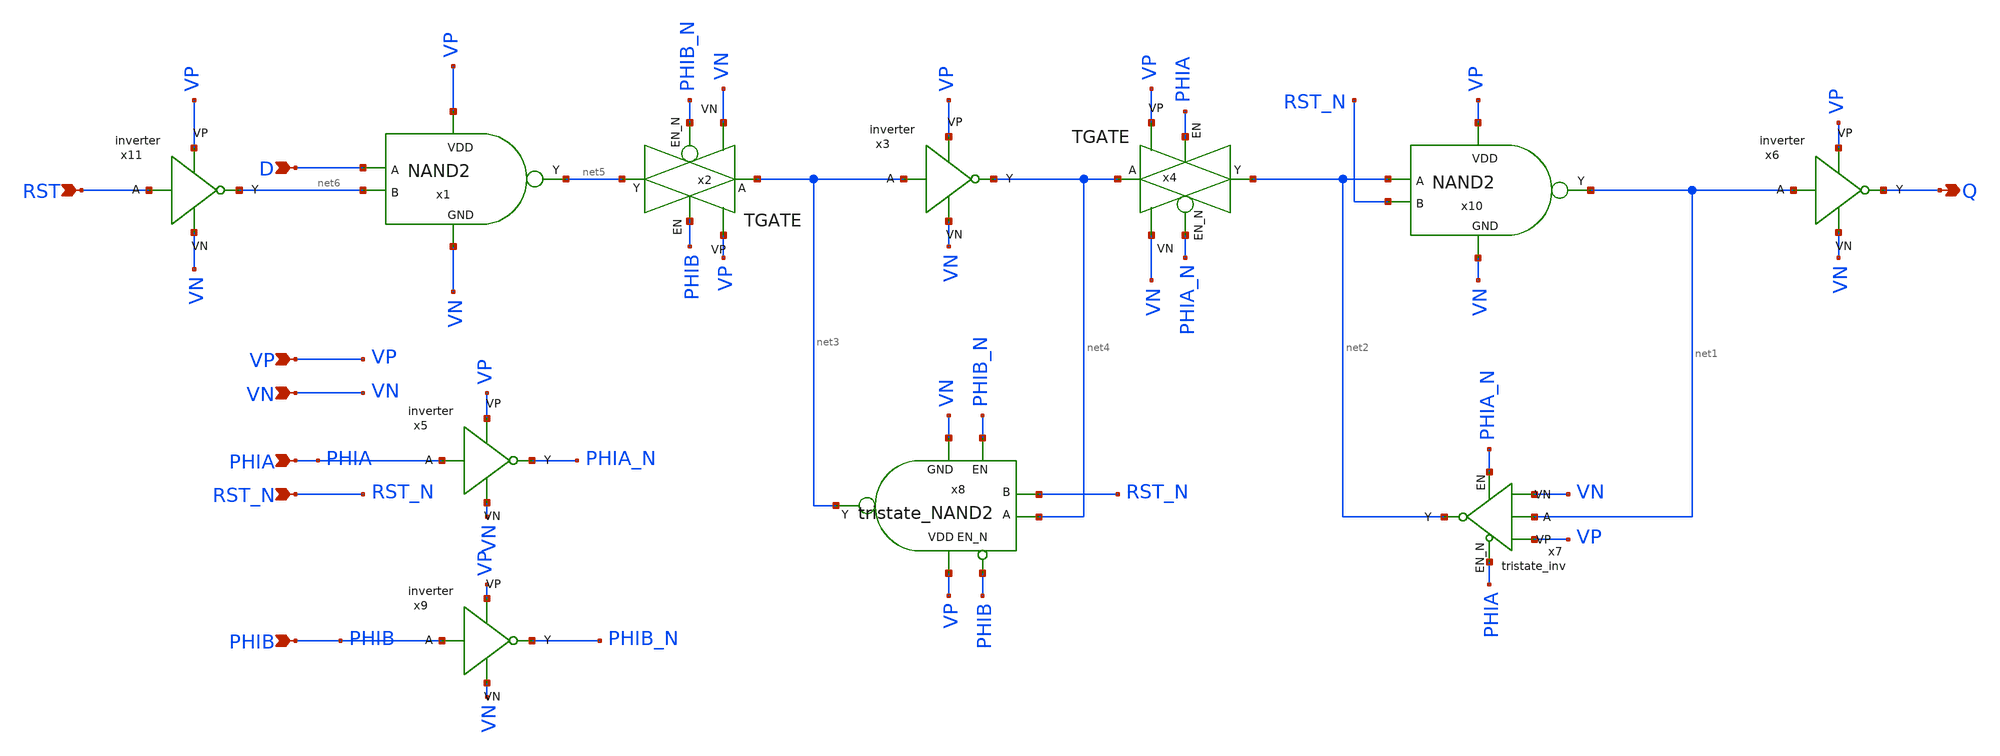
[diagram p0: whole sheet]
** sch_path: ADC/16bit_C2C/MagicAndSpice/EE431_FinalProj/DFFRNRS.sch
**.subckt DFFRNRS Q D VN RST_N VP PHIB PHIA RST
*.opin Q
*.ipin D
*.ipin VN
*.ipin RST_N
*.ipin VP
*.ipin PHIB
*.ipin PHIA
*.ipin RST
x2 net3 net5 PHIB PHIB_N TGATE
x3 net3 net4 VP VN inverter
x4 net4 net2 PHIA PHIA_N TGATE
x6 net1 Q VP VN inverter
x7 net1 net2 PHIA_N PHIA VP VN tristate_inv
x8 net4 RST_N net3 PHIB_N PHIB VP VN tristate_NAND2
x10 VP net1 net2 RST_N VN NAND2
x5 PHIA PHIA_N VP VN inverter
x9 PHIB PHIB_N VP VN inverter
x1 VP net5 D net6 VN NAND2
x11 RST net6 VP VN inverter
**.ends
.end
